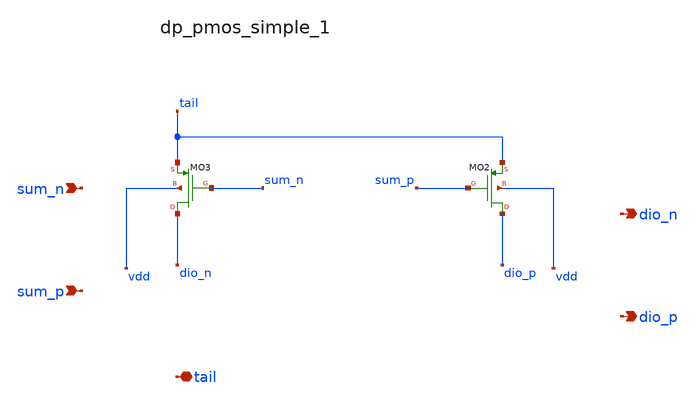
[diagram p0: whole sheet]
** sch_path: analog-db/raw/ia_001_hsu_bandpass_classab/hier/blocks/dp_pmos_simple_1.sch
**.subckt dp_pmos_simple_1 sum_n sum_p tail dio_n dio_p
*.ipin sum_n
*.ipin sum_p
*.iopin tail
*.opin dio_n
*.opin dio_p
XMO2 dio_p sum_p tail vdd sg13_lv_pmos w=x_dut_xmo2_w l=x_dut_xmo2_l ng=1 m=x_dut_xmo2_m
XMO3 dio_n sum_n tail vdd sg13_lv_pmos w=x_dut_xmo3_w l=x_dut_xmo3_l ng=1 m=x_dut_xmo3_m
**.ends
.end
